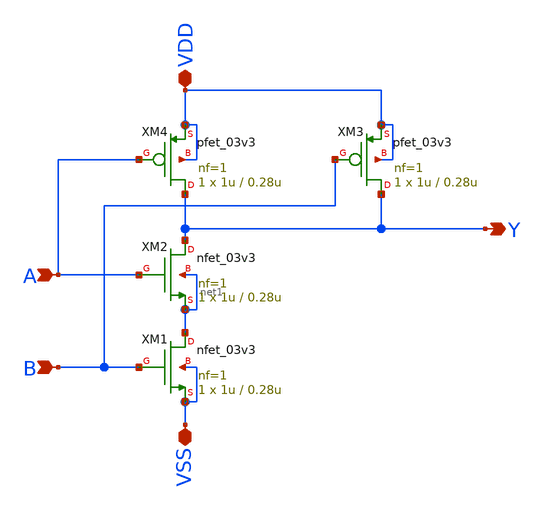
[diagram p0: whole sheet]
** sch_path: team_src/xschem/NAND_v1.sch
**.subckt NAND_v1 VSS VDD A Y B
*.iopin VSS
*.iopin VDD
*.ipin A
*.opin Y
*.ipin B
XM1 net1 B VSS VSS nfet_03v3 L=0.28u W=1u nf=1 ad='int((nf+1)/2) * W/nf * 0.18u' as='int((nf+2)/2) * W/nf * 0.18u'
+ pd='2*int((nf+1)/2) * (W/nf + 0.18u)' ps='2*int((nf+2)/2) * (W/nf + 0.18u)' nrd='0.18u / W' nrs='0.18u / W'
+ sa=0 sb=0 sd=0 m=1
XM2 Y A net1 net1 nfet_03v3 L=0.28u W=1u nf=1 ad='int((nf+1)/2) * W/nf * 0.18u' as='int((nf+2)/2) * W/nf * 0.18u'
+ pd='2*int((nf+1)/2) * (W/nf + 0.18u)' ps='2*int((nf+2)/2) * (W/nf + 0.18u)' nrd='0.18u / W' nrs='0.18u / W'
+ sa=0 sb=0 sd=0 m=1
XM3 Y B VDD VDD pfet_03v3 L=0.28u W=1u nf=1 ad='int((nf+1)/2) * W/nf * 0.18u' as='int((nf+2)/2) * W/nf * 0.18u'
+ pd='2*int((nf+1)/2) * (W/nf + 0.18u)' ps='2*int((nf+2)/2) * (W/nf + 0.18u)' nrd='0.18u / W' nrs='0.18u / W'
+ sa=0 sb=0 sd=0 m=1
XM4 Y A VDD VDD pfet_03v3 L=0.28u W=1u nf=1 ad='int((nf+1)/2) * W/nf * 0.18u' as='int((nf+2)/2) * W/nf * 0.18u'
+ pd='2*int((nf+1)/2) * (W/nf + 0.18u)' ps='2*int((nf+2)/2) * (W/nf + 0.18u)' nrd='0.18u / W' nrs='0.18u / W'
+ sa=0 sb=0 sd=0 m=1
**.ends
.end
